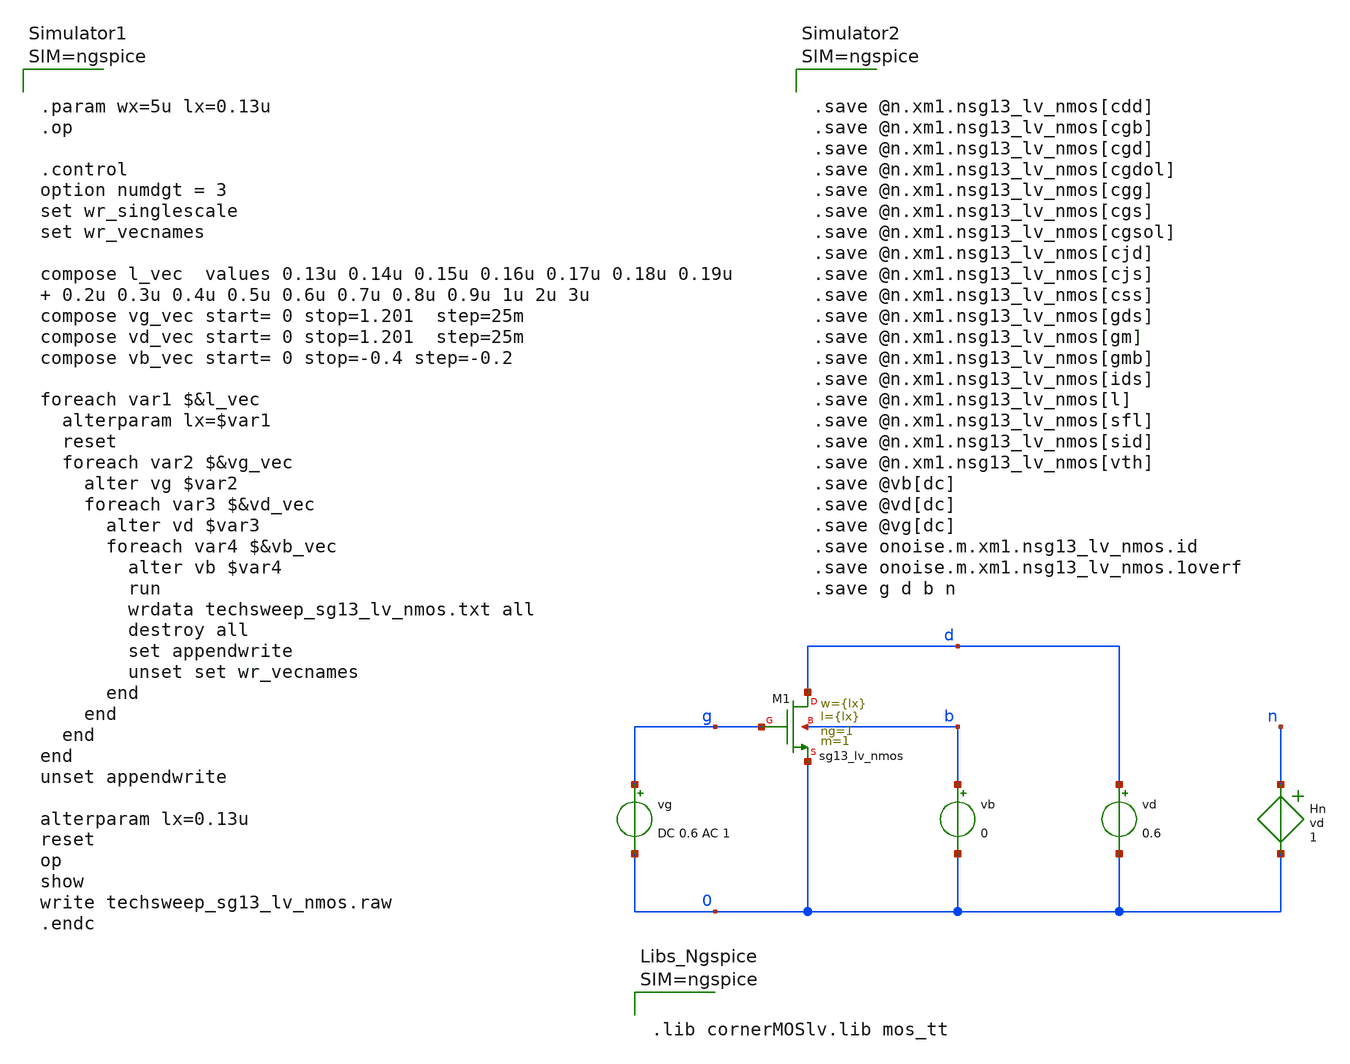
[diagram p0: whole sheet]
** sch_path: starter_files_open_source_tools/ihp-sg13cmos5l/techsweep_sg13_lv_nmos.sch
**.subckt techsweep_sg13_lv_nmos
vg g 0 DC 0.6 AC 1
vb b 0 0
vd d 0 0.6
Hn n 0 vd 1
XM1 d g 0 b sg13_lv_nmos w={lx} l={lx} ng=1 m=1 mm_ok=1
**** begin user architecture code



.save @n.xm1.nsg13_lv_nmos[cdd]
.save @n.xm1.nsg13_lv_nmos[cgb]
.save @n.xm1.nsg13_lv_nmos[cgd]
.save @n.xm1.nsg13_lv_nmos[cgdol]
.save @n.xm1.nsg13_lv_nmos[cgg]
.save @n.xm1.nsg13_lv_nmos[cgs]
.save @n.xm1.nsg13_lv_nmos[cgsol]
.save @n.xm1.nsg13_lv_nmos[cjd]
.save @n.xm1.nsg13_lv_nmos[cjs]
.save @n.xm1.nsg13_lv_nmos[css]
.save @n.xm1.nsg13_lv_nmos[gds]
.save @n.xm1.nsg13_lv_nmos[gm]
.save @n.xm1.nsg13_lv_nmos[gmb]
.save @n.xm1.nsg13_lv_nmos[ids]
.save @n.xm1.nsg13_lv_nmos[l]
.save @n.xm1.nsg13_lv_nmos[sfl]
.save @n.xm1.nsg13_lv_nmos[sid]
.save @n.xm1.nsg13_lv_nmos[vth]
.save @vb[dc]
.save @vd[dc]
.save @vg[dc]
.save onoise.m.xm1.nsg13_lv_nmos.id
.save onoise.m.xm1.nsg13_lv_nmos.1overf
.save g d b n






.param wx=5u lx=0.13u
.op

.control
option numdgt = 3
set wr_singlescale
set wr_vecnames

compose l_vec  values 0.13u 0.14u 0.15u 0.16u 0.17u 0.18u 0.19u  0.2u 0.3u 0.4u 0.5u 0.6u 0.7u 0.8u
+ 0.9u 1u 2u 3u
compose vg_vec start= 0 stop=1.201  step=25m
compose vd_vec start= 0 stop=1.201  step=25m
compose vb_vec start= 0 stop=-0.4 step=-0.2

foreach var1 $&l_vec
  alterparam lx=$var1
  reset
  foreach var2 $&vg_vec
    alter vg $var2
    foreach var3 $&vd_vec
      alter vd $var3
      foreach var4 $&vb_vec
        alter vb $var4
        run
        wrdata techsweep_sg13_lv_nmos.txt all
        destroy all
        set appendwrite
        unset set wr_vecnames
      end
    end
  end
end
unset appendwrite

alterparam lx=0.13u
reset
op
show
write techsweep_sg13_lv_nmos.raw
.endc






.lib cornerMOSlv.lib mos_tt



**** end user architecture code
**.ends
.end
